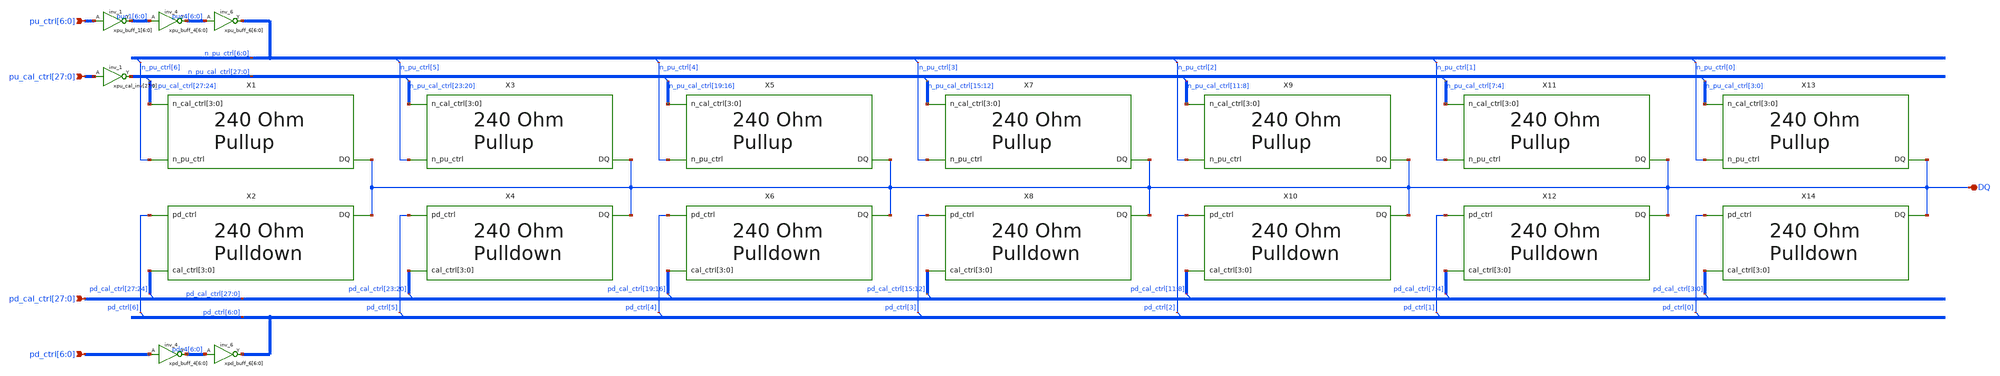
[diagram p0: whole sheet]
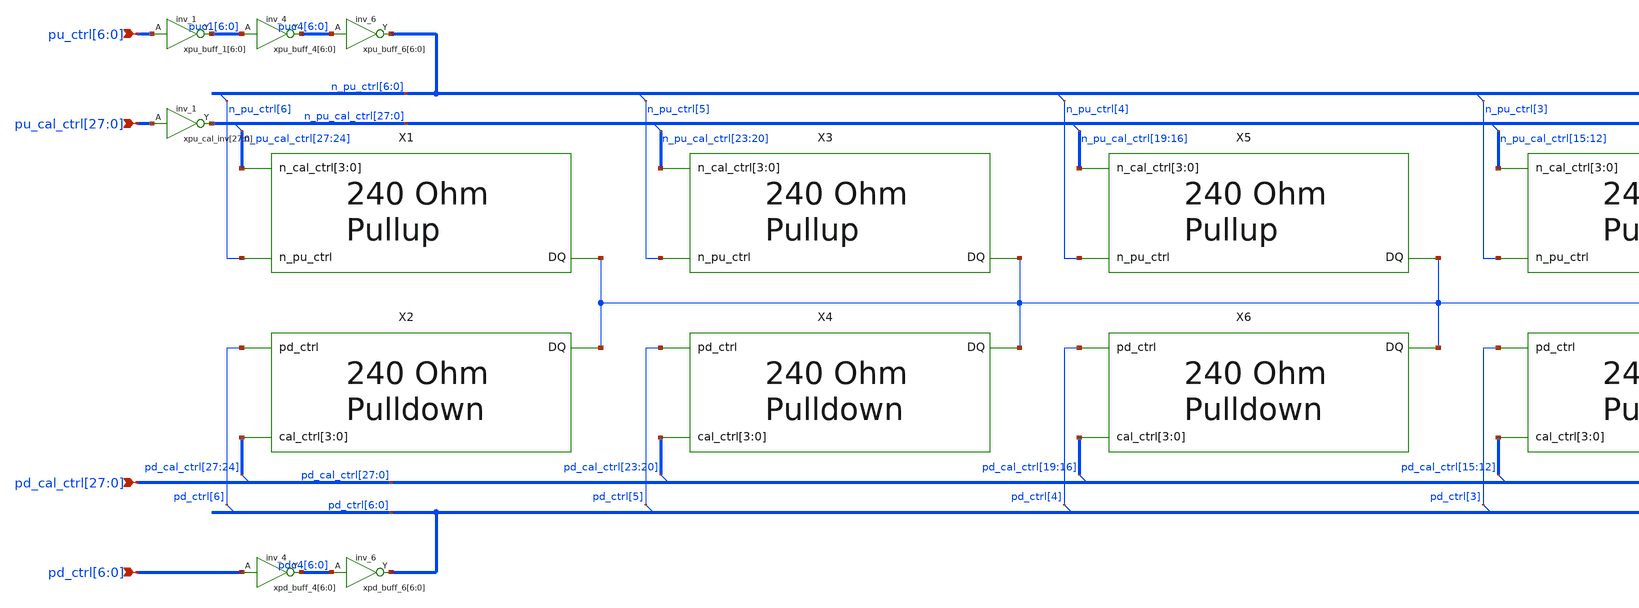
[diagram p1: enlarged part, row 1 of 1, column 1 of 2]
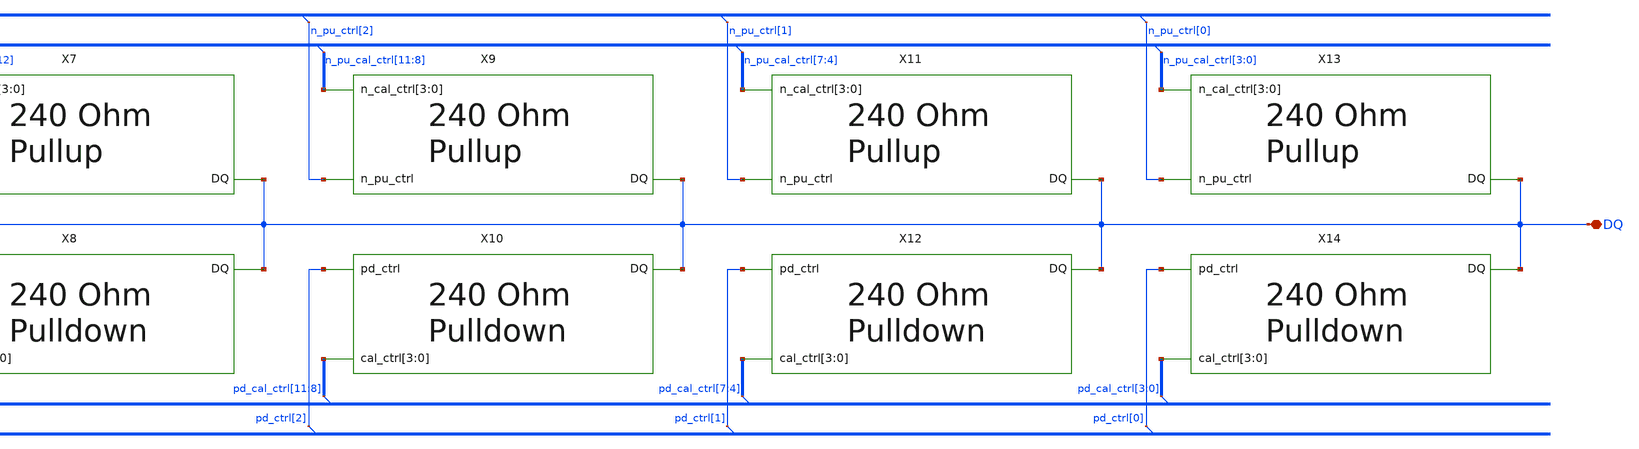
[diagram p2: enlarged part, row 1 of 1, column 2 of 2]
** sch_path: SSTL.sch
* Copyright 2021 Stefan Frederik Schippers
* Licensed under the Apache License, Version 2.0 (the "License");
* you may not use this file except in compliance with the License.
* You may obtain a copy of the License at
* https://www.apache.org/licenses/LICENSE-2.0
* Unless required by applicable law or agreed to in writing, software
* distributed under the License is distributed on an "AS IS" BASIS,
* WITHOUT WARRANTIES OR CONDITIONS OF ANY KIND, either express or implied.
* See the License for the specific language governing permissions and
* limitations under the License.
**.subckt SSTL DQ
*+ pu_cal_ctrl[27],pu_cal_ctrl[26],pu_cal_ctrl[25],pu_cal_ctrl[24],pu_cal_ctrl[23],pu_cal_ctrl[22],pu_cal_ctrl[21],pu_cal_ctrl[20],pu_cal_ctrl[19],pu_cal_ctrl[18],pu_cal_ctrl[17],pu_cal_ctrl[16],pu_cal_ctrl[15],pu_cal_ctrl[14],pu_cal_ctrl[13],pu_cal_ctrl[12],pu_cal_ctrl[11],pu_cal_ctrl[10],pu_cal_ctrl[9],pu_cal_ctrl[8],pu_cal_ctrl[7],pu_cal_ctrl[6],pu_cal_ctrl[5],pu_cal_ctrl[4],pu_cal_ctrl[3],pu_cal_ctrl[2],pu_cal_ctrl[1],pu_cal_ctrl[0]
*+ pd_cal_ctrl[27],pd_cal_ctrl[26],pd_cal_ctrl[25],pd_cal_ctrl[24],pd_cal_ctrl[23],pd_cal_ctrl[22],pd_cal_ctrl[21],pd_cal_ctrl[20],pd_cal_ctrl[19],pd_cal_ctrl[18],pd_cal_ctrl[17],pd_cal_ctrl[16],pd_cal_ctrl[15],pd_cal_ctrl[14],pd_cal_ctrl[13],pd_cal_ctrl[12],pd_cal_ctrl[11],pd_cal_ctrl[10],pd_cal_ctrl[9],pd_cal_ctrl[8],pd_cal_ctrl[7],pd_cal_ctrl[6],pd_cal_ctrl[5],pd_cal_ctrl[4],pd_cal_ctrl[3],pd_cal_ctrl[2],pd_cal_ctrl[1],pd_cal_ctrl[0] pu_ctrl[6],pu_ctrl[5],pu_ctrl[4],pu_ctrl[3],pu_ctrl[2],pu_ctrl[1],pu_ctrl[0]
*+ pd_ctrl[6],pd_ctrl[5],pd_ctrl[4],pd_ctrl[3],pd_ctrl[2],pd_ctrl[1],pd_ctrl[0]
*.iopin DQ
*.ipin
*+ pu_cal_ctrl[27],pu_cal_ctrl[26],pu_cal_ctrl[25],pu_cal_ctrl[24],pu_cal_ctrl[23],pu_cal_ctrl[22],pu_cal_ctrl[21],pu_cal_ctrl[20],pu_cal_ctrl[19],pu_cal_ctrl[18],pu_cal_ctrl[17],pu_cal_ctrl[16],pu_cal_ctrl[15],pu_cal_ctrl[14],pu_cal_ctrl[13],pu_cal_ctrl[12],pu_cal_ctrl[11],pu_cal_ctrl[10],pu_cal_ctrl[9],pu_cal_ctrl[8],pu_cal_ctrl[7],pu_cal_ctrl[6],pu_cal_ctrl[5],pu_cal_ctrl[4],pu_cal_ctrl[3],pu_cal_ctrl[2],pu_cal_ctrl[1],pu_cal_ctrl[0]
*.ipin
*+ pd_cal_ctrl[27],pd_cal_ctrl[26],pd_cal_ctrl[25],pd_cal_ctrl[24],pd_cal_ctrl[23],pd_cal_ctrl[22],pd_cal_ctrl[21],pd_cal_ctrl[20],pd_cal_ctrl[19],pd_cal_ctrl[18],pd_cal_ctrl[17],pd_cal_ctrl[16],pd_cal_ctrl[15],pd_cal_ctrl[14],pd_cal_ctrl[13],pd_cal_ctrl[12],pd_cal_ctrl[11],pd_cal_ctrl[10],pd_cal_ctrl[9],pd_cal_ctrl[8],pd_cal_ctrl[7],pd_cal_ctrl[6],pd_cal_ctrl[5],pd_cal_ctrl[4],pd_cal_ctrl[3],pd_cal_ctrl[2],pd_cal_ctrl[1],pd_cal_ctrl[0]
*.ipin pu_ctrl[6],pu_ctrl[5],pu_ctrl[4],pu_ctrl[3],pu_ctrl[2],pu_ctrl[1],pu_ctrl[0]
*.ipin pd_ctrl[6],pd_ctrl[5],pd_ctrl[4],pd_ctrl[3],pd_ctrl[2],pd_ctrl[1],pd_ctrl[0]
X1 DQ n_pu_ctrl[6] n_pu_cal_ctrl[27] n_pu_cal_ctrl[26] n_pu_cal_ctrl[25] n_pu_cal_ctrl[24] p-leg
X2 DQ pd_ctrl[6] pd_cal_ctrl[27] pd_cal_ctrl[26] pd_cal_ctrl[25] pd_cal_ctrl[24] n-leg
X3 DQ n_pu_ctrl[5] n_pu_cal_ctrl[23] n_pu_cal_ctrl[22] n_pu_cal_ctrl[21] n_pu_cal_ctrl[20] p-leg
X4 DQ pd_ctrl[5] pd_cal_ctrl[23] pd_cal_ctrl[22] pd_cal_ctrl[21] pd_cal_ctrl[20] n-leg
X5 DQ n_pu_ctrl[4] n_pu_cal_ctrl[19] n_pu_cal_ctrl[18] n_pu_cal_ctrl[17] n_pu_cal_ctrl[16] p-leg
X6 DQ pd_ctrl[4] pd_cal_ctrl[19] pd_cal_ctrl[18] pd_cal_ctrl[17] pd_cal_ctrl[16] n-leg
X7 DQ n_pu_ctrl[3] n_pu_cal_ctrl[15] n_pu_cal_ctrl[14] n_pu_cal_ctrl[13] n_pu_cal_ctrl[12] p-leg
X8 DQ pd_ctrl[3] pd_cal_ctrl[15] pd_cal_ctrl[14] pd_cal_ctrl[13] pd_cal_ctrl[12] n-leg
X9 DQ n_pu_ctrl[2] n_pu_cal_ctrl[11] n_pu_cal_ctrl[10] n_pu_cal_ctrl[9] n_pu_cal_ctrl[8] p-leg
X10 DQ pd_ctrl[2] pd_cal_ctrl[11] pd_cal_ctrl[10] pd_cal_ctrl[9] pd_cal_ctrl[8] n-leg
X11 DQ n_pu_ctrl[1] n_pu_cal_ctrl[7] n_pu_cal_ctrl[6] n_pu_cal_ctrl[5] n_pu_cal_ctrl[4] p-leg
X12 DQ pd_ctrl[1] pd_cal_ctrl[7] pd_cal_ctrl[6] pd_cal_ctrl[5] pd_cal_ctrl[4] n-leg
X13 DQ n_pu_ctrl[0] n_pu_cal_ctrl[3] n_pu_cal_ctrl[2] n_pu_cal_ctrl[1] n_pu_cal_ctrl[0] p-leg
X14 DQ pd_ctrl[0] pd_cal_ctrl[3] pd_cal_ctrl[2] pd_cal_ctrl[1] pd_cal_ctrl[0] n-leg
xpd_buff_4[6] pd_ctrl[6] VGND VNB VPB VPWR pdc4[6] sky130_fd_sc_hd__inv_4
xpd_buff_4[5] pd_ctrl[5] VGND VNB VPB VPWR pdc4[5] sky130_fd_sc_hd__inv_4
xpd_buff_4[4] pd_ctrl[4] VGND VNB VPB VPWR pdc4[4] sky130_fd_sc_hd__inv_4
xpd_buff_4[3] pd_ctrl[3] VGND VNB VPB VPWR pdc4[3] sky130_fd_sc_hd__inv_4
xpd_buff_4[2] pd_ctrl[2] VGND VNB VPB VPWR pdc4[2] sky130_fd_sc_hd__inv_4
xpd_buff_4[1] pd_ctrl[1] VGND VNB VPB VPWR pdc4[1] sky130_fd_sc_hd__inv_4
xpd_buff_4[0] pd_ctrl[0] VGND VNB VPB VPWR pdc4[0] sky130_fd_sc_hd__inv_4
xpd_buff_6[6] pdc4[6] VGND VNB VPB VPWR pd_ctrl[6] sky130_fd_sc_hd__inv_6
xpd_buff_6[5] pdc4[5] VGND VNB VPB VPWR pd_ctrl[5] sky130_fd_sc_hd__inv_6
xpd_buff_6[4] pdc4[4] VGND VNB VPB VPWR pd_ctrl[4] sky130_fd_sc_hd__inv_6
xpd_buff_6[3] pdc4[3] VGND VNB VPB VPWR pd_ctrl[3] sky130_fd_sc_hd__inv_6
xpd_buff_6[2] pdc4[2] VGND VNB VPB VPWR pd_ctrl[2] sky130_fd_sc_hd__inv_6
xpd_buff_6[1] pdc4[1] VGND VNB VPB VPWR pd_ctrl[1] sky130_fd_sc_hd__inv_6
xpd_buff_6[0] pdc4[0] VGND VNB VPB VPWR pd_ctrl[0] sky130_fd_sc_hd__inv_6
xpu_buff_4[6] puc1[6] VGND VNB VPB VPWR puc4[6] sky130_fd_sc_hd__inv_4
xpu_buff_4[5] puc1[5] VGND VNB VPB VPWR puc4[5] sky130_fd_sc_hd__inv_4
xpu_buff_4[4] puc1[4] VGND VNB VPB VPWR puc4[4] sky130_fd_sc_hd__inv_4
xpu_buff_4[3] puc1[3] VGND VNB VPB VPWR puc4[3] sky130_fd_sc_hd__inv_4
xpu_buff_4[2] puc1[2] VGND VNB VPB VPWR puc4[2] sky130_fd_sc_hd__inv_4
xpu_buff_4[1] puc1[1] VGND VNB VPB VPWR puc4[1] sky130_fd_sc_hd__inv_4
xpu_buff_4[0] puc1[0] VGND VNB VPB VPWR puc4[0] sky130_fd_sc_hd__inv_4
xpu_buff_6[6] puc4[6] VGND VNB VPB VPWR n_pu_ctrl[6] sky130_fd_sc_hd__inv_6
xpu_buff_6[5] puc4[5] VGND VNB VPB VPWR n_pu_ctrl[5] sky130_fd_sc_hd__inv_6
xpu_buff_6[4] puc4[4] VGND VNB VPB VPWR n_pu_ctrl[4] sky130_fd_sc_hd__inv_6
xpu_buff_6[3] puc4[3] VGND VNB VPB VPWR n_pu_ctrl[3] sky130_fd_sc_hd__inv_6
xpu_buff_6[2] puc4[2] VGND VNB VPB VPWR n_pu_ctrl[2] sky130_fd_sc_hd__inv_6
xpu_buff_6[1] puc4[1] VGND VNB VPB VPWR n_pu_ctrl[1] sky130_fd_sc_hd__inv_6
xpu_buff_6[0] puc4[0] VGND VNB VPB VPWR n_pu_ctrl[0] sky130_fd_sc_hd__inv_6
xpu_buff_1[6] pu_ctrl[6] VGND VNB VPB VPWR puc1[6] sky130_fd_sc_hd__inv_1
xpu_buff_1[5] pu_ctrl[5] VGND VNB VPB VPWR puc1[5] sky130_fd_sc_hd__inv_1
xpu_buff_1[4] pu_ctrl[4] VGND VNB VPB VPWR puc1[4] sky130_fd_sc_hd__inv_1
xpu_buff_1[3] pu_ctrl[3] VGND VNB VPB VPWR puc1[3] sky130_fd_sc_hd__inv_1
xpu_buff_1[2] pu_ctrl[2] VGND VNB VPB VPWR puc1[2] sky130_fd_sc_hd__inv_1
xpu_buff_1[1] pu_ctrl[1] VGND VNB VPB VPWR puc1[1] sky130_fd_sc_hd__inv_1
xpu_buff_1[0] pu_ctrl[0] VGND VNB VPB VPWR puc1[0] sky130_fd_sc_hd__inv_1
xpu_cal_inv[27] pu_cal_ctrl[27] VGND VNB VPB VPWR n_pu_cal_ctrl[27] sky130_fd_sc_hd__inv_1
xpu_cal_inv[26] pu_cal_ctrl[26] VGND VNB VPB VPWR n_pu_cal_ctrl[26] sky130_fd_sc_hd__inv_1
xpu_cal_inv[25] pu_cal_ctrl[25] VGND VNB VPB VPWR n_pu_cal_ctrl[25] sky130_fd_sc_hd__inv_1
xpu_cal_inv[24] pu_cal_ctrl[24] VGND VNB VPB VPWR n_pu_cal_ctrl[24] sky130_fd_sc_hd__inv_1
xpu_cal_inv[23] pu_cal_ctrl[23] VGND VNB VPB VPWR n_pu_cal_ctrl[23] sky130_fd_sc_hd__inv_1
xpu_cal_inv[22] pu_cal_ctrl[22] VGND VNB VPB VPWR n_pu_cal_ctrl[22] sky130_fd_sc_hd__inv_1
xpu_cal_inv[21] pu_cal_ctrl[21] VGND VNB VPB VPWR n_pu_cal_ctrl[21] sky130_fd_sc_hd__inv_1
xpu_cal_inv[20] pu_cal_ctrl[20] VGND VNB VPB VPWR n_pu_cal_ctrl[20] sky130_fd_sc_hd__inv_1
xpu_cal_inv[19] pu_cal_ctrl[19] VGND VNB VPB VPWR n_pu_cal_ctrl[19] sky130_fd_sc_hd__inv_1
xpu_cal_inv[18] pu_cal_ctrl[18] VGND VNB VPB VPWR n_pu_cal_ctrl[18] sky130_fd_sc_hd__inv_1
xpu_cal_inv[17] pu_cal_ctrl[17] VGND VNB VPB VPWR n_pu_cal_ctrl[17] sky130_fd_sc_hd__inv_1
xpu_cal_inv[16] pu_cal_ctrl[16] VGND VNB VPB VPWR n_pu_cal_ctrl[16] sky130_fd_sc_hd__inv_1
xpu_cal_inv[15] pu_cal_ctrl[15] VGND VNB VPB VPWR n_pu_cal_ctrl[15] sky130_fd_sc_hd__inv_1
xpu_cal_inv[14] pu_cal_ctrl[14] VGND VNB VPB VPWR n_pu_cal_ctrl[14] sky130_fd_sc_hd__inv_1
xpu_cal_inv[13] pu_cal_ctrl[13] VGND VNB VPB VPWR n_pu_cal_ctrl[13] sky130_fd_sc_hd__inv_1
xpu_cal_inv[12] pu_cal_ctrl[12] VGND VNB VPB VPWR n_pu_cal_ctrl[12] sky130_fd_sc_hd__inv_1
xpu_cal_inv[11] pu_cal_ctrl[11] VGND VNB VPB VPWR n_pu_cal_ctrl[11] sky130_fd_sc_hd__inv_1
xpu_cal_inv[10] pu_cal_ctrl[10] VGND VNB VPB VPWR n_pu_cal_ctrl[10] sky130_fd_sc_hd__inv_1
xpu_cal_inv[9] pu_cal_ctrl[9] VGND VNB VPB VPWR n_pu_cal_ctrl[9] sky130_fd_sc_hd__inv_1
xpu_cal_inv[8] pu_cal_ctrl[8] VGND VNB VPB VPWR n_pu_cal_ctrl[8] sky130_fd_sc_hd__inv_1
xpu_cal_inv[7] pu_cal_ctrl[7] VGND VNB VPB VPWR n_pu_cal_ctrl[7] sky130_fd_sc_hd__inv_1
xpu_cal_inv[6] pu_cal_ctrl[6] VGND VNB VPB VPWR n_pu_cal_ctrl[6] sky130_fd_sc_hd__inv_1
xpu_cal_inv[5] pu_cal_ctrl[5] VGND VNB VPB VPWR n_pu_cal_ctrl[5] sky130_fd_sc_hd__inv_1
xpu_cal_inv[4] pu_cal_ctrl[4] VGND VNB VPB VPWR n_pu_cal_ctrl[4] sky130_fd_sc_hd__inv_1
xpu_cal_inv[3] pu_cal_ctrl[3] VGND VNB VPB VPWR n_pu_cal_ctrl[3] sky130_fd_sc_hd__inv_1
xpu_cal_inv[2] pu_cal_ctrl[2] VGND VNB VPB VPWR n_pu_cal_ctrl[2] sky130_fd_sc_hd__inv_1
xpu_cal_inv[1] pu_cal_ctrl[1] VGND VNB VPB VPWR n_pu_cal_ctrl[1] sky130_fd_sc_hd__inv_1
xpu_cal_inv[0] pu_cal_ctrl[0] VGND VNB VPB VPWR n_pu_cal_ctrl[0] sky130_fd_sc_hd__inv_1
**.ends
.end
